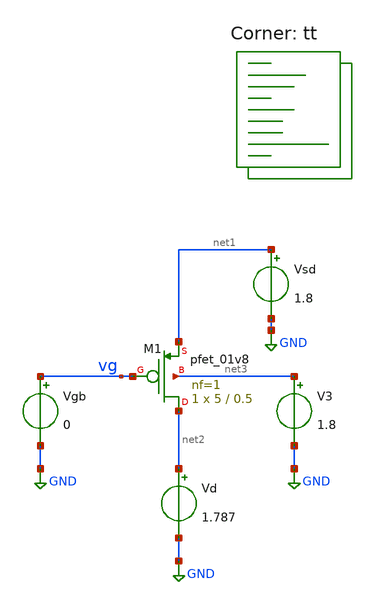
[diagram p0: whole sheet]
** sch_path: legacy/Examples/SkyWater130/xschem/Extraction/pmos_ext.sch
**.subckt pmos_ext
Vgb vg GND 0
Vsd net1 GND 1.8
V3 net3 GND 1.8
Vd net2 GND 1.787
XM1 net2 vg net1 net3 sky130_fd_pr__pfet_01v8 L=0.5 W=5 nf=1 ad='int((nf+1)/2) * W/nf * 0.29' as='int((nf+2)/2) * W/nf * 0.29'
+ pd='2*int((nf+1)/2) * (W/nf + 0.29)' ps='2*int((nf+2)/2) * (W/nf + 0.29)' nrd='0.29 / W' nrs='0.29 / W'
+ sa=0 sb=0 sd=0 mult=1 m=1
**** begin user architecture code
.lib $::SKYWATER_MODELS/sky130.lib.spice tt



.control
save all
dc Vgb 0.05 2.5 20m

let gm_id = -deriv(ln(i(Vd)))
save gm_id

meas dc gm_id_max MAX gm_id
let gm_id_vt = 0.531*gm_id_max
save gm_id_vt

meas dc vt FIND V(vg) WHEN gm_id=gm_id_vt
let vt0=vt-1.8
meas dc is0_ FIND i(Vd) WHEN V(vg)=vt

let is0 = is0_/0.88
let VT_val=0.026
let n = 1/(gm_id_max*VT_val)
save is0 vt0 n
echo
echo
echo

echo Extracted parameters:
print is0 vt0 n


echo
echo
echo

remzerovec
write pmos_ext.raw

.endc



**** end user architecture code
**.ends
.GLOBAL GND
.end
